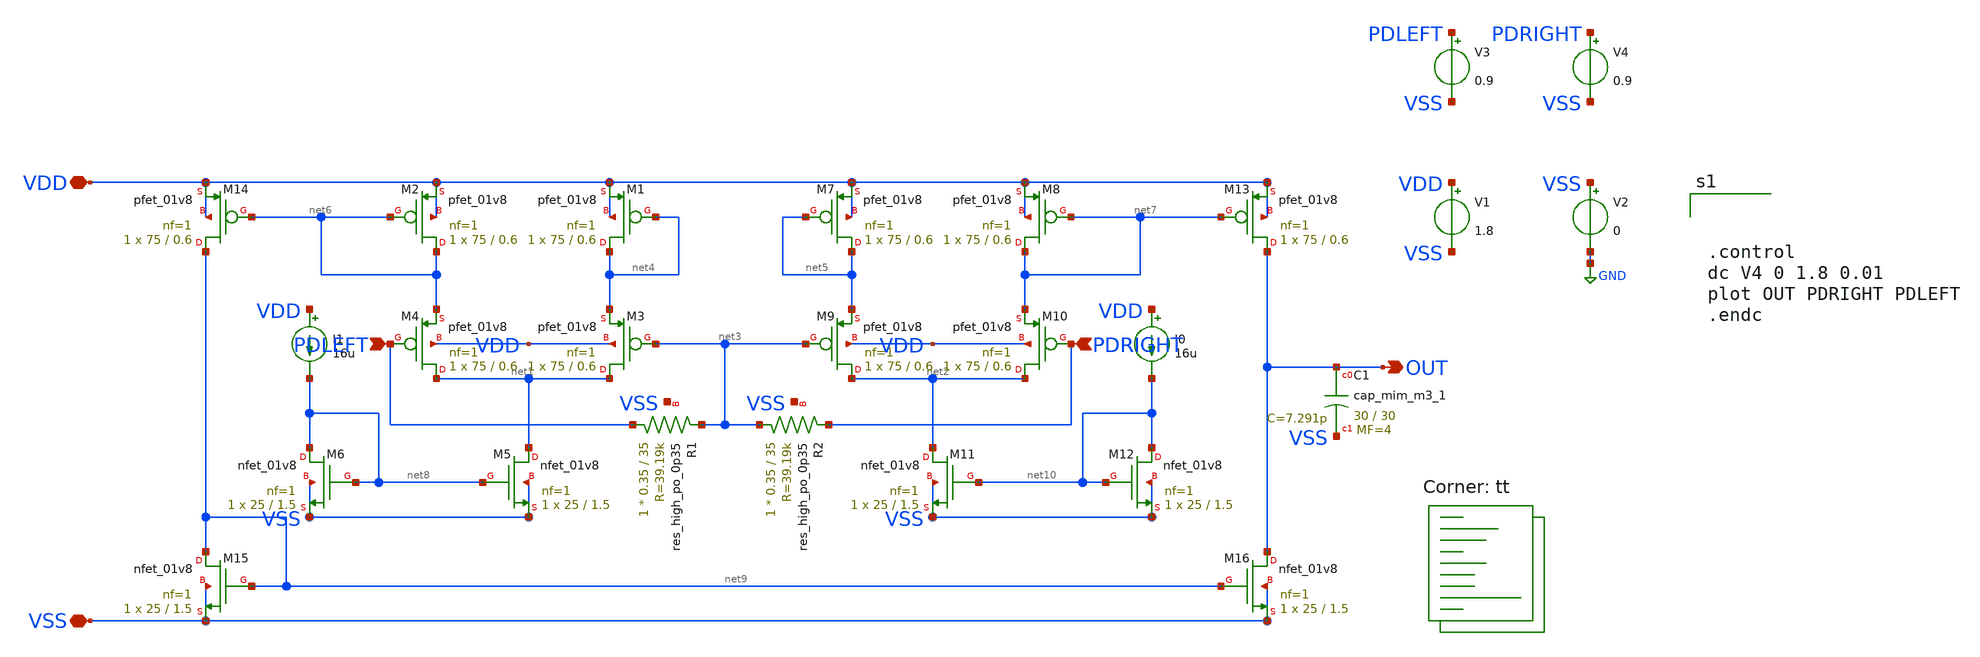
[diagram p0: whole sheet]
** sch_path: CTLE/voltage-to-i-converter.sch
**.subckt voltage-to-i-converter VDD VSS OUT PDRIGHT PDLEFT PDRIGHT
*.iopin VDD
*.iopin VSS
*.opin OUT
*.ipin PDRIGHT
*.ipin PDLEFT
*.ipin PDRIGHT
XM1 net4 net4 VDD VDD sky130_fd_pr__pfet_01v8 L=0.6 W=75 nf=1 ad='int((nf+1)/2) * W/nf * 0.29' as='int((nf+2)/2) * W/nf * 0.29'
+ pd='2*int((nf+1)/2) * (W/nf + 0.29)' ps='2*int((nf+2)/2) * (W/nf + 0.29)' nrd='0.29 / W' nrs='0.29 / W'
+ sa=0 sb=0 sd=0 mult=1 m=1
XM2 net6 net6 VDD VDD sky130_fd_pr__pfet_01v8 L=0.6 W=75 nf=1 ad='int((nf+1)/2) * W/nf * 0.29' as='int((nf+2)/2) * W/nf * 0.29'
+ pd='2*int((nf+1)/2) * (W/nf + 0.29)' ps='2*int((nf+2)/2) * (W/nf + 0.29)' nrd='0.29 / W' nrs='0.29 / W'
+ sa=0 sb=0 sd=0 mult=1 m=1
XM3 net1 net3 net4 VDD sky130_fd_pr__pfet_01v8 L=0.6 W=75 nf=1 ad='int((nf+1)/2) * W/nf * 0.29' as='int((nf+2)/2) * W/nf * 0.29'
+ pd='2*int((nf+1)/2) * (W/nf + 0.29)' ps='2*int((nf+2)/2) * (W/nf + 0.29)' nrd='0.29 / W' nrs='0.29 / W'
+ sa=0 sb=0 sd=0 mult=1 m=1
XM4 net1 PDLEFT net6 VDD sky130_fd_pr__pfet_01v8 L=0.6 W=75 nf=1 ad='int((nf+1)/2) * W/nf * 0.29' as='int((nf+2)/2) * W/nf * 0.29'
+ pd='2*int((nf+1)/2) * (W/nf + 0.29)' ps='2*int((nf+2)/2) * (W/nf + 0.29)' nrd='0.29 / W' nrs='0.29 / W'
+ sa=0 sb=0 sd=0 mult=1 m=1
XM5 net1 net8 VSS VSS sky130_fd_pr__nfet_01v8 L=1.5 W=25 nf=1 ad='int((nf+1)/2) * W/nf * 0.29' as='int((nf+2)/2) * W/nf * 0.29'
+ pd='2*int((nf+1)/2) * (W/nf + 0.29)' ps='2*int((nf+2)/2) * (W/nf + 0.29)' nrd='0.29 / W' nrs='0.29 / W'
+ sa=0 sb=0 sd=0 mult=1 m=1
XM6 net8 net8 VSS VSS sky130_fd_pr__nfet_01v8 L=1.5 W=25 nf=1 ad='int((nf+1)/2) * W/nf * 0.29' as='int((nf+2)/2) * W/nf * 0.29'
+ pd='2*int((nf+1)/2) * (W/nf + 0.29)' ps='2*int((nf+2)/2) * (W/nf + 0.29)' nrd='0.29 / W' nrs='0.29 / W'
+ sa=0 sb=0 sd=0 mult=1 m=1
XM7 net5 net5 VDD VDD sky130_fd_pr__pfet_01v8 L=0.6 W=75 nf=1 ad='int((nf+1)/2) * W/nf * 0.29' as='int((nf+2)/2) * W/nf * 0.29'
+ pd='2*int((nf+1)/2) * (W/nf + 0.29)' ps='2*int((nf+2)/2) * (W/nf + 0.29)' nrd='0.29 / W' nrs='0.29 / W'
+ sa=0 sb=0 sd=0 mult=1 m=1
XM8 net7 net7 VDD VDD sky130_fd_pr__pfet_01v8 L=0.6 W=75 nf=1 ad='int((nf+1)/2) * W/nf * 0.29' as='int((nf+2)/2) * W/nf * 0.29'
+ pd='2*int((nf+1)/2) * (W/nf + 0.29)' ps='2*int((nf+2)/2) * (W/nf + 0.29)' nrd='0.29 / W' nrs='0.29 / W'
+ sa=0 sb=0 sd=0 mult=1 m=1
XM9 net2 net3 net5 VDD sky130_fd_pr__pfet_01v8 L=0.6 W=75 nf=1 ad='int((nf+1)/2) * W/nf * 0.29' as='int((nf+2)/2) * W/nf * 0.29'
+ pd='2*int((nf+1)/2) * (W/nf + 0.29)' ps='2*int((nf+2)/2) * (W/nf + 0.29)' nrd='0.29 / W' nrs='0.29 / W'
+ sa=0 sb=0 sd=0 mult=1 m=1
XM10 net2 PDRIGHT net7 VDD sky130_fd_pr__pfet_01v8 L=0.6 W=75 nf=1 ad='int((nf+1)/2) * W/nf * 0.29' as='int((nf+2)/2) * W/nf * 0.29'
+ pd='2*int((nf+1)/2) * (W/nf + 0.29)' ps='2*int((nf+2)/2) * (W/nf + 0.29)' nrd='0.29 / W' nrs='0.29 / W'
+ sa=0 sb=0 sd=0 mult=1 m=1
XM11 net2 net10 VSS VSS sky130_fd_pr__nfet_01v8 L=1.5 W=25 nf=1 ad='int((nf+1)/2) * W/nf * 0.29' as='int((nf+2)/2) * W/nf * 0.29'
+ pd='2*int((nf+1)/2) * (W/nf + 0.29)' ps='2*int((nf+2)/2) * (W/nf + 0.29)' nrd='0.29 / W' nrs='0.29 / W'
+ sa=0 sb=0 sd=0 mult=1 m=1
XM12 net10 net10 VSS VSS sky130_fd_pr__nfet_01v8 L=1.5 W=25 nf=1 ad='int((nf+1)/2) * W/nf * 0.29' as='int((nf+2)/2) * W/nf * 0.29'
+ pd='2*int((nf+1)/2) * (W/nf + 0.29)' ps='2*int((nf+2)/2) * (W/nf + 0.29)' nrd='0.29 / W' nrs='0.29 / W'
+ sa=0 sb=0 sd=0 mult=1 m=1
XM13 OUT net7 VDD VDD sky130_fd_pr__pfet_01v8 L=0.6 W=75 nf=1 ad='int((nf+1)/2) * W/nf * 0.29' as='int((nf+2)/2) * W/nf * 0.29'
+ pd='2*int((nf+1)/2) * (W/nf + 0.29)' ps='2*int((nf+2)/2) * (W/nf + 0.29)' nrd='0.29 / W' nrs='0.29 / W'
+ sa=0 sb=0 sd=0 mult=1 m=1
XM14 net9 net6 VDD VDD sky130_fd_pr__pfet_01v8 L=0.6 W=75 nf=1 ad='int((nf+1)/2) * W/nf * 0.29' as='int((nf+2)/2) * W/nf * 0.29'
+ pd='2*int((nf+1)/2) * (W/nf + 0.29)' ps='2*int((nf+2)/2) * (W/nf + 0.29)' nrd='0.29 / W' nrs='0.29 / W'
+ sa=0 sb=0 sd=0 mult=1 m=1
XM15 net9 net9 VSS VSS sky130_fd_pr__nfet_01v8 L=1.5 W=25 nf=1 ad='int((nf+1)/2) * W/nf * 0.29' as='int((nf+2)/2) * W/nf * 0.29'
+ pd='2*int((nf+1)/2) * (W/nf + 0.29)' ps='2*int((nf+2)/2) * (W/nf + 0.29)' nrd='0.29 / W' nrs='0.29 / W'
+ sa=0 sb=0 sd=0 mult=1 m=1
XM16 OUT net9 VSS VSS sky130_fd_pr__nfet_01v8 L=1.5 W=25 nf=1 ad='int((nf+1)/2) * W/nf * 0.29' as='int((nf+2)/2) * W/nf * 0.29'
+ pd='2*int((nf+1)/2) * (W/nf + 0.29)' ps='2*int((nf+2)/2) * (W/nf + 0.29)' nrd='0.29 / W' nrs='0.29 / W'
+ sa=0 sb=0 sd=0 mult=1 m=1
XR1 PDLEFT net3 VSS sky130_fd_pr__res_high_po_0p35 L=35 mult=1 m=1
XR2 net3 PDRIGHT VSS sky130_fd_pr__res_high_po_0p35 L=35 mult=1 m=1
I0 VDD net10 16u
I1 VDD net8 16u
XC1 OUT VSS sky130_fd_pr__cap_mim_m3_1 W=30 L=30 MF=4 m=4
V1 VDD VSS 1.8
V2 VSS GND 0
V3 PDLEFT VSS 0.9
V4 PDRIGHT VSS 0.9
**** begin user architecture code
.lib $::SKYWATER_MODELS/sky130.lib.spice tt



.control
dc V4 0 1.8 0.01
plot OUT PDRIGHT PDLEFT
.endc


**** end user architecture code
**.ends
.GLOBAL GND
.end
